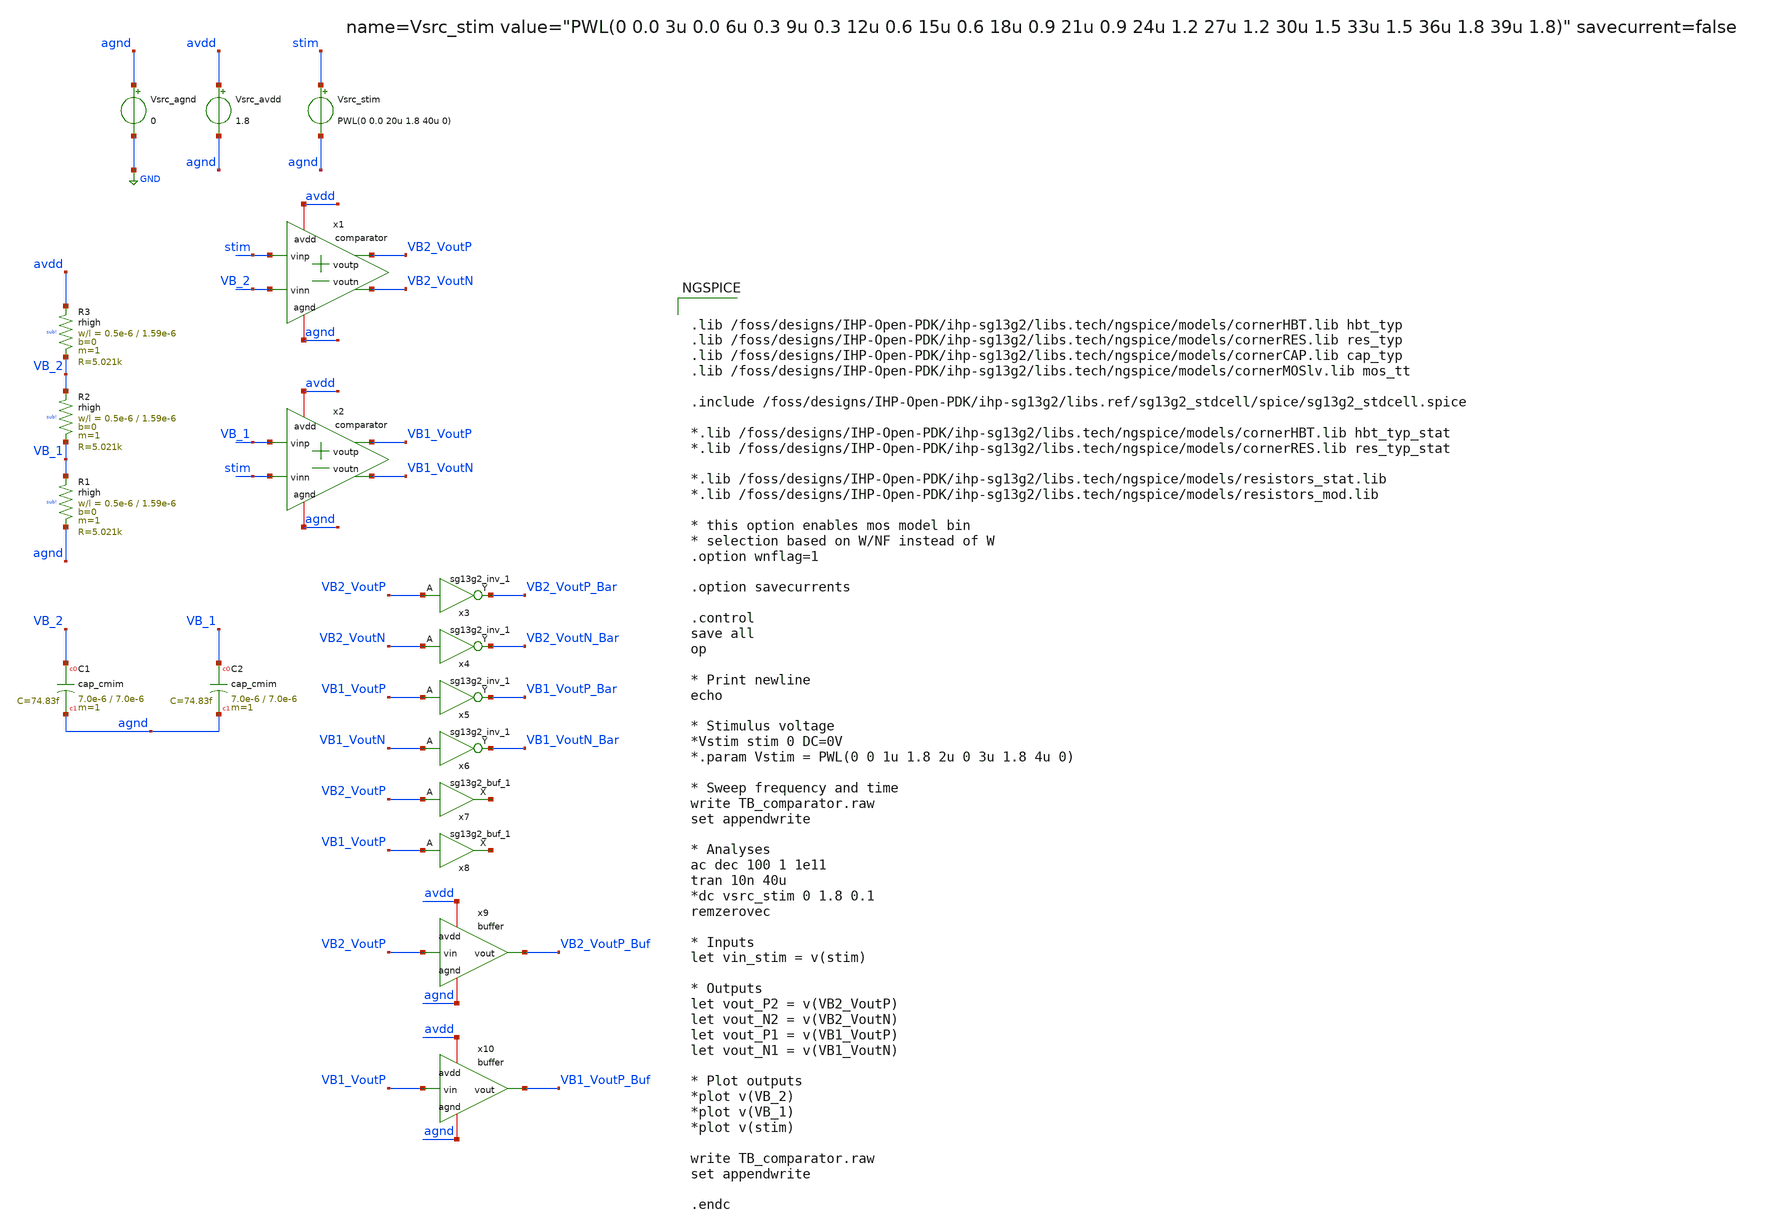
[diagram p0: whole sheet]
** sch_path: xschem/TB_comparator.sch
* IHP-GmbH/IHP-Open-PDK/ihp-sg13g2/libs.tech/xschem/sg13g2_stdcells/sg13g2_buf_1.sch:
* Copyright 2023 IHP PDK Authors
* Licensed under the Apache License, Version 2.0 (the "License");
**.subckt TB_comparator
x1 avdd VB2_VoutP VB2_VoutN VB_2 stim agnd comparator
Vsrc_agnd agnd GND 0
Vsrc_avdd avdd agnd 1.8
x2 avdd VB1_VoutP VB1_VoutN stim VB_1 agnd comparator
XR3 avdd VB_2 sub! rhigh w=0.5e-6 l=1.59e-6 m=1 b=0 mm_ok=1
Vsrc_stim stim agnd PWL(0 0.0 20u 1.8 40u 0)
XR1 VB_1 agnd sub! rhigh w=0.5e-6 l=1.59e-6 m=1 b=0 mm_ok=1
XR2 VB_2 VB_1 sub! rhigh w=0.5e-6 l=1.59e-6 m=1 b=0 mm_ok=1
XC1 VB_2 agnd cap_cmim w=7.0e-6 l=7.0e-6 m=1 mm_ok=1
XC2 VB_1 agnd cap_cmim w=7.0e-6 l=7.0e-6 m=1 mm_ok=1
x3 VB2_VoutP_Bar VB2_VoutP avdd agnd sg13g2_inv_1
x4 VB2_VoutN_Bar VB2_VoutN avdd agnd sg13g2_inv_1
x5 VB1_VoutP_Bar VB1_VoutP avdd agnd sg13g2_inv_1
x6 VB1_VoutN_Bar VB1_VoutN avdd agnd sg13g2_inv_1
x7 net1 VB2_VoutP avdd agnd sg13g2_buf_1
x8 net2 VB1_VoutP avdd agnd sg13g2_buf_1
x9 avdd VB2_VoutP VB2_VoutP_Buf agnd buffer
x10 avdd VB1_VoutP VB1_VoutP_Buf agnd buffer
**** begin user architecture code


.lib /foss/designs/IHP-Open-PDK/ihp-sg13g2/libs.tech/ngspice/models/cornerHBT.lib hbt_typ
.lib /foss/designs/IHP-Open-PDK/ihp-sg13g2/libs.tech/ngspice/models/cornerRES.lib res_typ
.lib /foss/designs/IHP-Open-PDK/ihp-sg13g2/libs.tech/ngspice/models/cornerCAP.lib cap_typ
.lib /foss/designs/IHP-Open-PDK/ihp-sg13g2/libs.tech/ngspice/models/cornerMOSlv.lib mos_tt

.include /foss/designs/IHP-Open-PDK/ihp-sg13g2/libs.ref/sg13g2_stdcell/spice/sg13g2_stdcell.spice

*.lib /foss/designs/IHP-Open-PDK/ihp-sg13g2/libs.tech/ngspice/models/cornerHBT.lib hbt_typ_stat
*.lib /foss/designs/IHP-Open-PDK/ihp-sg13g2/libs.tech/ngspice/models/cornerRES.lib res_typ_stat

*.lib /foss/designs/IHP-Open-PDK/ihp-sg13g2/libs.tech/ngspice/models/resistors_stat.lib
*.lib /foss/designs/IHP-Open-PDK/ihp-sg13g2/libs.tech/ngspice/models/resistors_mod.lib

* this option enables mos model bin
* selection based on W/NF instead of W
.option wnflag=1

.option savecurrents

.control
save all
op

* Print newline
echo

* Stimulus voltage
*Vstim stim 0 DC=0V
*.param Vstim = PWL(0 0 1u 1.8 2u 0 3u 1.8 4u 0)

* Sweep frequency and time
write TB_comparator.raw
set appendwrite

* Analyses
ac dec 100 1 1e11
tran 10n 40u
*dc vsrc_stim 0 1.8 0.1
remzerovec

* Inputs
let vin_stim = v(stim)

* Outputs
let vout_P2 = v(VB2_VoutP)
let vout_N2 = v(VB2_VoutN)
let vout_P1 = v(VB1_VoutP)
let vout_N1 = v(VB1_VoutN)

* Plot outputs
*plot v(VB_2)
*plot v(VB_1)
*plot v(stim)

write TB_comparator.raw
set appendwrite

.endc


**** end user architecture code
**.ends

* expanding   symbol:  comparator.sym # of pins=6
** sym_path: xschem/comparator.sym
** sch_path: xschem/comparator.sch
.subckt comparator avdd voutp voutn vinn vinp agnd
*.iopin avdd
*.ipin vinp
*.opin voutp
*.iopin agnd
*.ipin vinn
*.opin voutn
XQ1 voutp vinn ee agnd npn13G2 Nx=1 mm_ok=1
XR1 avdd voutp sub! rppd w=0.5e-6 l=30e-6 m=1 b=0 mm_ok=1
XR2 ee agnd sub! rppd w=0.5e-6 l=0.5e-6 m=1 b=0 mm_ok=1
XR3 avdd voutn sub! rppd w=0.5e-6 l=30e-6 m=1 b=0 mm_ok=1
XQ2 voutn vinp ee agnd npn13G2 Nx=1 mm_ok=1
.ends


* expanding   symbol:  sg13g2_stdcells/sg13g2_inv_1.sym # of pins=2
** sym_path: sg13g2_stdcells/sg13g2_inv_1.sym
** sch_path: sg13g2_stdcells/sg13g2_inv_1.sch
.subckt sg13g2_inv_1 Y A VDD VSS
*.opin Y
*.ipin A
*.iopin VDD
*.iopin VSS
XM1 Y A VSS VSS sg13_lv_nmos w=740.00n l=130.00n ng=1 m=1 mm_ok=1
XM2 Y A VDD VDD sg13_lv_pmos w=1.12u l=130.00n ng=1 m=1 mm_ok=1
.ends


* expanding   symbol:  sg13g2_stdcells/sg13g2_buf_1.sym # of pins=2
** sym_path: sg13g2_stdcells/sg13g2_buf_1.sym
** sch_path: sg13g2_stdcells/sg13g2_buf_1.sch
.subckt sg13g2_buf_1 X A VDD VSS
*.ipin A
*.opin X
*.iopin VDD
*.iopin VSS
XM1 net1 A VSS VSS sg13_lv_nmos w=550.00n l=130.00n ng=1 m=1 mm_ok=1
XM2 X net1 VSS VSS sg13_lv_nmos w=740.00n l=130.00n ng=1 m=1 mm_ok=1
XM3 net1 A VDD VDD sg13_lv_pmos w=840.00n l=130.00n ng=1 m=1 mm_ok=1
XM4 X net1 VDD VDD sg13_lv_pmos w=1.12u l=130.00n ng=1 m=1 mm_ok=1
.ends


* expanding   symbol:  buffer.sym # of pins=4
** sym_path: xschem/buffer.sym
** sch_path: xschem/buffer.sch
.subckt buffer avdd vin vout agnd
*.iopin avdd
*.ipin vin
*.opin vout
*.iopin agnd
x1 avdd vin net1 agnd inverter
x2 avdd net1 vout agnd inverter
.ends


* expanding   symbol:  inverter.sym # of pins=4
** sym_path: xschem/inverter.sym
** sch_path: xschem/inverter.sch
.subckt inverter avdd vin vout agnd
*.iopin avdd
*.ipin vin
*.opin vout
*.iopin agnd
XQ1 vout base agnd agnd npn13G2 Nx=10 mm_ok=1
XR1 avdd vout sub! rhigh w=1e-6 l=0.5e-6 m=1 b=0 mm_ok=1
XR2 base vin sub! rhigh w=0.5e-6 l=0.5e-6 m=1 b=0 mm_ok=1
.ends

.GLOBAL GND
.end
